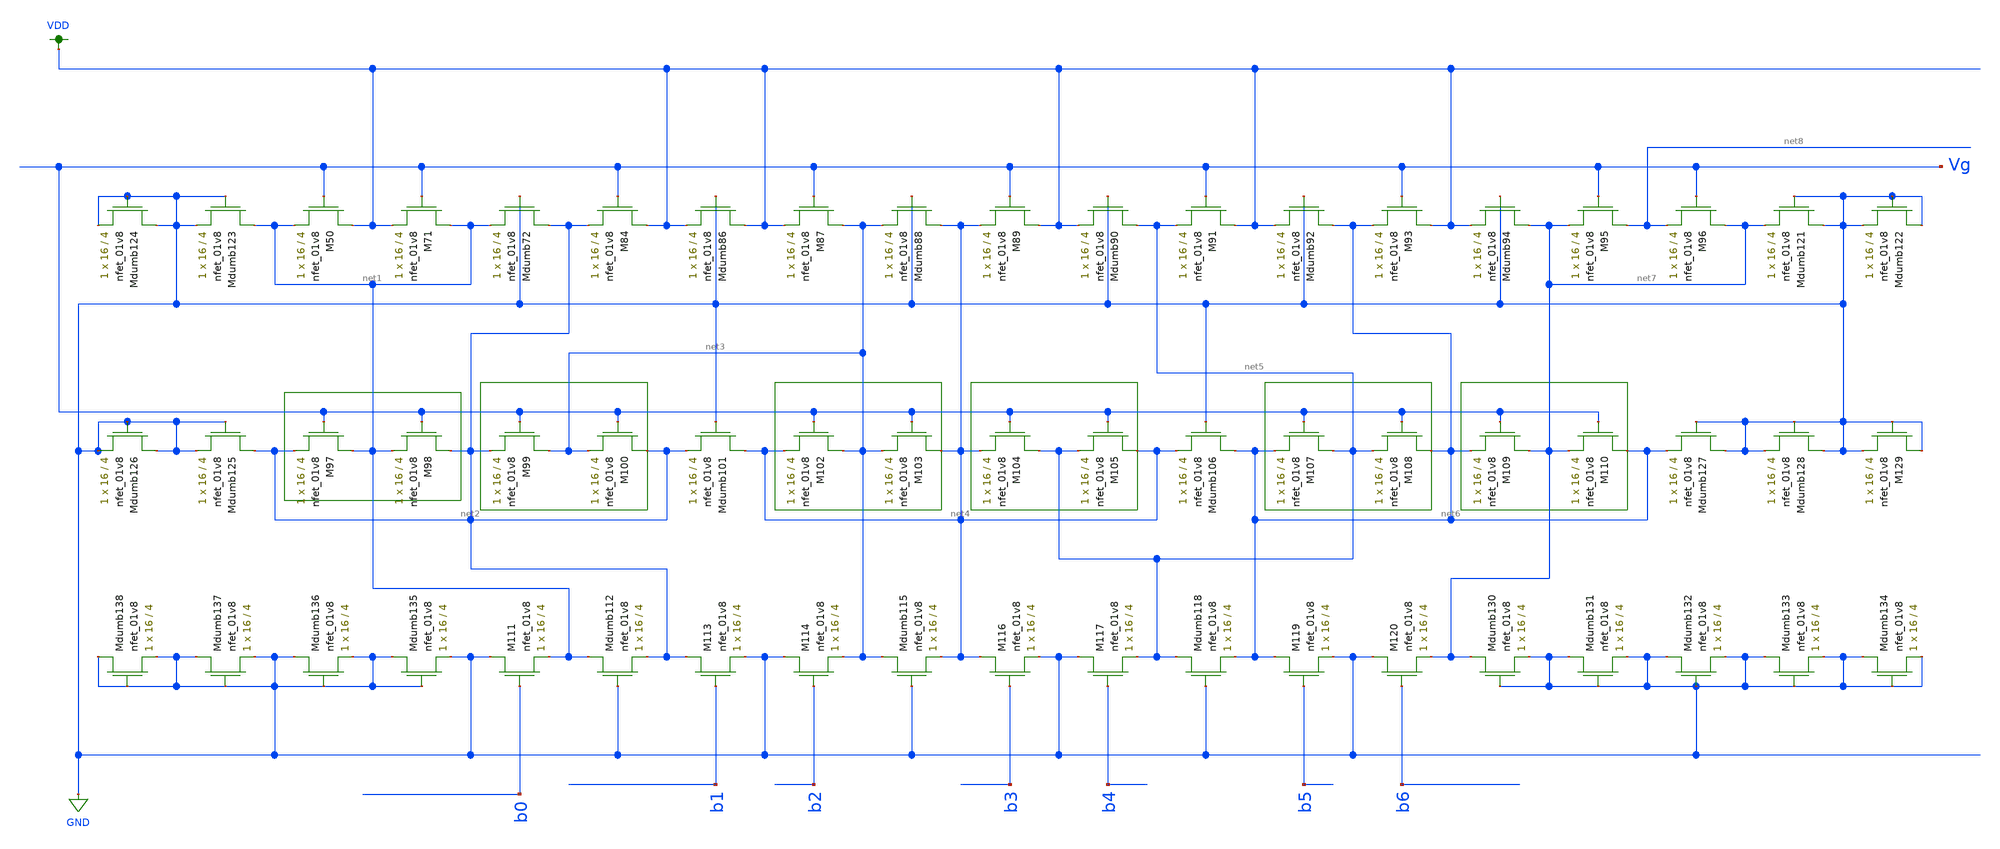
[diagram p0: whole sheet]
** sch_path: schematic/LDS/ladder_lds.sch
**.subckt ladder_lds
XM50 VDD Vg net1 GND sky130_fd_pr__nfet_01v8 L=4 W=16 nf=1 ad='int((nf+1)/2) * W/nf * 0.29' as='int((nf+2)/2) * W/nf * 0.29'
+ pd='2*int((nf+1)/2) * (W/nf + 0.29)' ps='2*int((nf+2)/2) * (W/nf + 0.29)' nrd='0.29 / W' nrs='0.29 / W'
+ sa=0 sb=0 sd=0 mult=1 m=1
XM71 net1 Vg VDD GND sky130_fd_pr__nfet_01v8 L=4 W=16 nf=1 ad='int((nf+1)/2) * W/nf * 0.29' as='int((nf+2)/2) * W/nf * 0.29'
+ pd='2*int((nf+1)/2) * (W/nf + 0.29)' ps='2*int((nf+2)/2) * (W/nf + 0.29)' nrd='0.29 / W' nrs='0.29 / W'
+ sa=0 sb=0 sd=0 mult=1 m=1
XMdumb72 net2 GND net1 GND sky130_fd_pr__nfet_01v8 L=4 W=16 nf=1 ad='int((nf+1)/2) * W/nf * 0.29' as='int((nf+2)/2) * W/nf * 0.29'
+ pd='2*int((nf+1)/2) * (W/nf + 0.29)' ps='2*int((nf+2)/2) * (W/nf + 0.29)' nrd='0.29 / W' nrs='0.29 / W'
+ sa=0 sb=0 sd=0 mult=1 m=1
XM84 VDD Vg net2 GND sky130_fd_pr__nfet_01v8 L=4 W=16 nf=1 ad='int((nf+1)/2) * W/nf * 0.29' as='int((nf+2)/2) * W/nf * 0.29'
+ pd='2*int((nf+1)/2) * (W/nf + 0.29)' ps='2*int((nf+2)/2) * (W/nf + 0.29)' nrd='0.29 / W' nrs='0.29 / W'
+ sa=0 sb=0 sd=0 mult=1 m=1
XMdumb86 VDD GND VDD GND sky130_fd_pr__nfet_01v8 L=4 W=16 nf=1 ad='int((nf+1)/2) * W/nf * 0.29' as='int((nf+2)/2) * W/nf * 0.29'
+ pd='2*int((nf+1)/2) * (W/nf + 0.29)' ps='2*int((nf+2)/2) * (W/nf + 0.29)' nrd='0.29 / W' nrs='0.29 / W'
+ sa=0 sb=0 sd=0 mult=1 m=1
XM87 net3 Vg VDD GND sky130_fd_pr__nfet_01v8 L=4 W=16 nf=1 ad='int((nf+1)/2) * W/nf * 0.29' as='int((nf+2)/2) * W/nf * 0.29'
+ pd='2*int((nf+1)/2) * (W/nf + 0.29)' ps='2*int((nf+2)/2) * (W/nf + 0.29)' nrd='0.29 / W' nrs='0.29 / W'
+ sa=0 sb=0 sd=0 mult=1 m=1
XMdumb88 net4 GND net3 GND sky130_fd_pr__nfet_01v8 L=4 W=16 nf=1 ad='int((nf+1)/2) * W/nf * 0.29' as='int((nf+2)/2) * W/nf * 0.29'
+ pd='2*int((nf+1)/2) * (W/nf + 0.29)' ps='2*int((nf+2)/2) * (W/nf + 0.29)' nrd='0.29 / W' nrs='0.29 / W'
+ sa=0 sb=0 sd=0 mult=1 m=1
XM89 VDD Vg net4 GND sky130_fd_pr__nfet_01v8 L=4 W=16 nf=1 ad='int((nf+1)/2) * W/nf * 0.29' as='int((nf+2)/2) * W/nf * 0.29'
+ pd='2*int((nf+1)/2) * (W/nf + 0.29)' ps='2*int((nf+2)/2) * (W/nf + 0.29)' nrd='0.29 / W' nrs='0.29 / W'
+ sa=0 sb=0 sd=0 mult=1 m=1
XMdumb90 net5 GND VDD GND sky130_fd_pr__nfet_01v8 L=4 W=16 nf=1 ad='int((nf+1)/2) * W/nf * 0.29' as='int((nf+2)/2) * W/nf * 0.29'
+ pd='2*int((nf+1)/2) * (W/nf + 0.29)' ps='2*int((nf+2)/2) * (W/nf + 0.29)' nrd='0.29 / W' nrs='0.29 / W'
+ sa=0 sb=0 sd=0 mult=1 m=1
XM91 VDD Vg net5 GND sky130_fd_pr__nfet_01v8 L=4 W=16 nf=1 ad='int((nf+1)/2) * W/nf * 0.29' as='int((nf+2)/2) * W/nf * 0.29'
+ pd='2*int((nf+1)/2) * (W/nf + 0.29)' ps='2*int((nf+2)/2) * (W/nf + 0.29)' nrd='0.29 / W' nrs='0.29 / W'
+ sa=0 sb=0 sd=0 mult=1 m=1
XMdumb92 net6 GND VDD GND sky130_fd_pr__nfet_01v8 L=4 W=16 nf=1 ad='int((nf+1)/2) * W/nf * 0.29' as='int((nf+2)/2) * W/nf * 0.29'
+ pd='2*int((nf+1)/2) * (W/nf + 0.29)' ps='2*int((nf+2)/2) * (W/nf + 0.29)' nrd='0.29 / W' nrs='0.29 / W'
+ sa=0 sb=0 sd=0 mult=1 m=1
XM93 VDD Vg net6 GND sky130_fd_pr__nfet_01v8 L=4 W=16 nf=1 ad='int((nf+1)/2) * W/nf * 0.29' as='int((nf+2)/2) * W/nf * 0.29'
+ pd='2*int((nf+1)/2) * (W/nf + 0.29)' ps='2*int((nf+2)/2) * (W/nf + 0.29)' nrd='0.29 / W' nrs='0.29 / W'
+ sa=0 sb=0 sd=0 mult=1 m=1
XMdumb94 net7 GND VDD GND sky130_fd_pr__nfet_01v8 L=4 W=16 nf=1 ad='int((nf+1)/2) * W/nf * 0.29' as='int((nf+2)/2) * W/nf * 0.29'
+ pd='2*int((nf+1)/2) * (W/nf + 0.29)' ps='2*int((nf+2)/2) * (W/nf + 0.29)' nrd='0.29 / W' nrs='0.29 / W'
+ sa=0 sb=0 sd=0 mult=1 m=1
XM95 net8 Vg net7 GND sky130_fd_pr__nfet_01v8 L=4 W=16 nf=1 ad='int((nf+1)/2) * W/nf * 0.29' as='int((nf+2)/2) * W/nf * 0.29'
+ pd='2*int((nf+1)/2) * (W/nf + 0.29)' ps='2*int((nf+2)/2) * (W/nf + 0.29)' nrd='0.29 / W' nrs='0.29 / W'
+ sa=0 sb=0 sd=0 mult=1 m=1
XM96 net7 Vg net8 GND sky130_fd_pr__nfet_01v8 L=4 W=16 nf=1 ad='int((nf+1)/2) * W/nf * 0.29' as='int((nf+2)/2) * W/nf * 0.29'
+ pd='2*int((nf+1)/2) * (W/nf + 0.29)' ps='2*int((nf+2)/2) * (W/nf + 0.29)' nrd='0.29 / W' nrs='0.29 / W'
+ sa=0 sb=0 sd=0 mult=1 m=1
XM97 net1 Vg net2 GND sky130_fd_pr__nfet_01v8 L=4 W=16 nf=1 ad='int((nf+1)/2) * W/nf * 0.29' as='int((nf+2)/2) * W/nf * 0.29'
+ pd='2*int((nf+1)/2) * (W/nf + 0.29)' ps='2*int((nf+2)/2) * (W/nf + 0.29)' nrd='0.29 / W' nrs='0.29 / W'
+ sa=0 sb=0 sd=0 mult=1 m=1
XM98 net2 Vg net1 GND sky130_fd_pr__nfet_01v8 L=4 W=16 nf=1 ad='int((nf+1)/2) * W/nf * 0.29' as='int((nf+2)/2) * W/nf * 0.29'
+ pd='2*int((nf+1)/2) * (W/nf + 0.29)' ps='2*int((nf+2)/2) * (W/nf + 0.29)' nrd='0.29 / W' nrs='0.29 / W'
+ sa=0 sb=0 sd=0 mult=1 m=1
XM99 net3 Vg net2 GND sky130_fd_pr__nfet_01v8 L=4 W=16 nf=1 ad='int((nf+1)/2) * W/nf * 0.29' as='int((nf+2)/2) * W/nf * 0.29'
+ pd='2*int((nf+1)/2) * (W/nf + 0.29)' ps='2*int((nf+2)/2) * (W/nf + 0.29)' nrd='0.29 / W' nrs='0.29 / W'
+ sa=0 sb=0 sd=0 mult=1 m=1
XM100 net2 Vg net3 GND sky130_fd_pr__nfet_01v8 L=4 W=16 nf=1 ad='int((nf+1)/2) * W/nf * 0.29' as='int((nf+2)/2) * W/nf * 0.29'
+ pd='2*int((nf+1)/2) * (W/nf + 0.29)' ps='2*int((nf+2)/2) * (W/nf + 0.29)' nrd='0.29 / W' nrs='0.29 / W'
+ sa=0 sb=0 sd=0 mult=1 m=1
XMdumb101 net4 GND net2 GND sky130_fd_pr__nfet_01v8 L=4 W=16 nf=1 ad='int((nf+1)/2) * W/nf * 0.29' as='int((nf+2)/2) * W/nf * 0.29'
+ pd='2*int((nf+1)/2) * (W/nf + 0.29)' ps='2*int((nf+2)/2) * (W/nf + 0.29)' nrd='0.29 / W' nrs='0.29 / W'
+ sa=0 sb=0 sd=0 mult=1 m=1
XM102 net3 Vg net4 GND sky130_fd_pr__nfet_01v8 L=4 W=16 nf=1 ad='int((nf+1)/2) * W/nf * 0.29' as='int((nf+2)/2) * W/nf * 0.29'
+ pd='2*int((nf+1)/2) * (W/nf + 0.29)' ps='2*int((nf+2)/2) * (W/nf + 0.29)' nrd='0.29 / W' nrs='0.29 / W'
+ sa=0 sb=0 sd=0 mult=1 m=1
XM103 net4 Vg net3 GND sky130_fd_pr__nfet_01v8 L=4 W=16 nf=1 ad='int((nf+1)/2) * W/nf * 0.29' as='int((nf+2)/2) * W/nf * 0.29'
+ pd='2*int((nf+1)/2) * (W/nf + 0.29)' ps='2*int((nf+2)/2) * (W/nf + 0.29)' nrd='0.29 / W' nrs='0.29 / W'
+ sa=0 sb=0 sd=0 mult=1 m=1
XM104 net5 Vg net4 GND sky130_fd_pr__nfet_01v8 L=4 W=16 nf=1 ad='int((nf+1)/2) * W/nf * 0.29' as='int((nf+2)/2) * W/nf * 0.29'
+ pd='2*int((nf+1)/2) * (W/nf + 0.29)' ps='2*int((nf+2)/2) * (W/nf + 0.29)' nrd='0.29 / W' nrs='0.29 / W'
+ sa=0 sb=0 sd=0 mult=1 m=1
XM105 net4 Vg net5 GND sky130_fd_pr__nfet_01v8 L=4 W=16 nf=1 ad='int((nf+1)/2) * W/nf * 0.29' as='int((nf+2)/2) * W/nf * 0.29'
+ pd='2*int((nf+1)/2) * (W/nf + 0.29)' ps='2*int((nf+2)/2) * (W/nf + 0.29)' nrd='0.29 / W' nrs='0.29 / W'
+ sa=0 sb=0 sd=0 mult=1 m=1
XMdumb106 net6 GND net4 GND sky130_fd_pr__nfet_01v8 L=4 W=16 nf=1 ad='int((nf+1)/2) * W/nf * 0.29' as='int((nf+2)/2) * W/nf * 0.29'
+ pd='2*int((nf+1)/2) * (W/nf + 0.29)' ps='2*int((nf+2)/2) * (W/nf + 0.29)' nrd='0.29 / W' nrs='0.29 / W'
+ sa=0 sb=0 sd=0 mult=1 m=1
XM107 net5 Vg net6 GND sky130_fd_pr__nfet_01v8 L=4 W=16 nf=1 ad='int((nf+1)/2) * W/nf * 0.29' as='int((nf+2)/2) * W/nf * 0.29'
+ pd='2*int((nf+1)/2) * (W/nf + 0.29)' ps='2*int((nf+2)/2) * (W/nf + 0.29)' nrd='0.29 / W' nrs='0.29 / W'
+ sa=0 sb=0 sd=0 mult=1 m=1
XM108 net6 Vg net5 GND sky130_fd_pr__nfet_01v8 L=4 W=16 nf=1 ad='int((nf+1)/2) * W/nf * 0.29' as='int((nf+2)/2) * W/nf * 0.29'
+ pd='2*int((nf+1)/2) * (W/nf + 0.29)' ps='2*int((nf+2)/2) * (W/nf + 0.29)' nrd='0.29 / W' nrs='0.29 / W'
+ sa=0 sb=0 sd=0 mult=1 m=1
XM109 net7 Vg net6 GND sky130_fd_pr__nfet_01v8 L=4 W=16 nf=1 ad='int((nf+1)/2) * W/nf * 0.29' as='int((nf+2)/2) * W/nf * 0.29'
+ pd='2*int((nf+1)/2) * (W/nf + 0.29)' ps='2*int((nf+2)/2) * (W/nf + 0.29)' nrd='0.29 / W' nrs='0.29 / W'
+ sa=0 sb=0 sd=0 mult=1 m=1
XM110 net6 Vg net7 GND sky130_fd_pr__nfet_01v8 L=4 W=16 nf=1 ad='int((nf+1)/2) * W/nf * 0.29' as='int((nf+2)/2) * W/nf * 0.29'
+ pd='2*int((nf+1)/2) * (W/nf + 0.29)' ps='2*int((nf+2)/2) * (W/nf + 0.29)' nrd='0.29 / W' nrs='0.29 / W'
+ sa=0 sb=0 sd=0 mult=1 m=1
XM111 GND b0 net1 GND sky130_fd_pr__nfet_01v8 L=4 W=16 nf=1 ad='int((nf+1)/2) * W/nf * 0.29' as='int((nf+2)/2) * W/nf * 0.29'
+ pd='2*int((nf+1)/2) * (W/nf + 0.29)' ps='2*int((nf+2)/2) * (W/nf + 0.29)' nrd='0.29 / W' nrs='0.29 / W'
+ sa=0 sb=0 sd=0 mult=1 m=1
XMdumb112 net1 GND net2 GND sky130_fd_pr__nfet_01v8 L=4 W=16 nf=1 ad='int((nf+1)/2) * W/nf * 0.29' as='int((nf+2)/2) * W/nf * 0.29'
+ pd='2*int((nf+1)/2) * (W/nf + 0.29)' ps='2*int((nf+2)/2) * (W/nf + 0.29)' nrd='0.29 / W' nrs='0.29 / W'
+ sa=0 sb=0 sd=0 mult=1 m=1
XM113 net2 b1 GND GND sky130_fd_pr__nfet_01v8 L=4 W=16 nf=1 ad='int((nf+1)/2) * W/nf * 0.29' as='int((nf+2)/2) * W/nf * 0.29'
+ pd='2*int((nf+1)/2) * (W/nf + 0.29)' ps='2*int((nf+2)/2) * (W/nf + 0.29)' nrd='0.29 / W' nrs='0.29 / W'
+ sa=0 sb=0 sd=0 mult=1 m=1
XM114 GND b2 net3 GND sky130_fd_pr__nfet_01v8 L=4 W=16 nf=1 ad='int((nf+1)/2) * W/nf * 0.29' as='int((nf+2)/2) * W/nf * 0.29'
+ pd='2*int((nf+1)/2) * (W/nf + 0.29)' ps='2*int((nf+2)/2) * (W/nf + 0.29)' nrd='0.29 / W' nrs='0.29 / W'
+ sa=0 sb=0 sd=0 mult=1 m=1
XMdumb115 net3 GND net4 GND sky130_fd_pr__nfet_01v8 L=4 W=16 nf=1 ad='int((nf+1)/2) * W/nf * 0.29' as='int((nf+2)/2) * W/nf * 0.29'
+ pd='2*int((nf+1)/2) * (W/nf + 0.29)' ps='2*int((nf+2)/2) * (W/nf + 0.29)' nrd='0.29 / W' nrs='0.29 / W'
+ sa=0 sb=0 sd=0 mult=1 m=1
XM116 net4 b3 GND GND sky130_fd_pr__nfet_01v8 L=4 W=16 nf=1 ad='int((nf+1)/2) * W/nf * 0.29' as='int((nf+2)/2) * W/nf * 0.29'
+ pd='2*int((nf+1)/2) * (W/nf + 0.29)' ps='2*int((nf+2)/2) * (W/nf + 0.29)' nrd='0.29 / W' nrs='0.29 / W'
+ sa=0 sb=0 sd=0 mult=1 m=1
XM117 GND b4 net5 GND sky130_fd_pr__nfet_01v8 L=4 W=16 nf=1 ad='int((nf+1)/2) * W/nf * 0.29' as='int((nf+2)/2) * W/nf * 0.29'
+ pd='2*int((nf+1)/2) * (W/nf + 0.29)' ps='2*int((nf+2)/2) * (W/nf + 0.29)' nrd='0.29 / W' nrs='0.29 / W'
+ sa=0 sb=0 sd=0 mult=1 m=1
XMdumb118 net5 GND net6 GND sky130_fd_pr__nfet_01v8 L=4 W=16 nf=1 ad='int((nf+1)/2) * W/nf * 0.29' as='int((nf+2)/2) * W/nf * 0.29'
+ pd='2*int((nf+1)/2) * (W/nf + 0.29)' ps='2*int((nf+2)/2) * (W/nf + 0.29)' nrd='0.29 / W' nrs='0.29 / W'
+ sa=0 sb=0 sd=0 mult=1 m=1
XM119 net6 b5 GND GND sky130_fd_pr__nfet_01v8 L=4 W=16 nf=1 ad='int((nf+1)/2) * W/nf * 0.29' as='int((nf+2)/2) * W/nf * 0.29'
+ pd='2*int((nf+1)/2) * (W/nf + 0.29)' ps='2*int((nf+2)/2) * (W/nf + 0.29)' nrd='0.29 / W' nrs='0.29 / W'
+ sa=0 sb=0 sd=0 mult=1 m=1
XM120 GND b6 net7 GND sky130_fd_pr__nfet_01v8 L=4 W=16 nf=1 ad='int((nf+1)/2) * W/nf * 0.29' as='int((nf+2)/2) * W/nf * 0.29'
+ pd='2*int((nf+1)/2) * (W/nf + 0.29)' ps='2*int((nf+2)/2) * (W/nf + 0.29)' nrd='0.29 / W' nrs='0.29 / W'
+ sa=0 sb=0 sd=0 mult=1 m=1
XMdumb121 GND GND net7 GND sky130_fd_pr__nfet_01v8 L=4 W=16 nf=1 ad='int((nf+1)/2) * W/nf * 0.29' as='int((nf+2)/2) * W/nf * 0.29'
+ pd='2*int((nf+1)/2) * (W/nf + 0.29)' ps='2*int((nf+2)/2) * (W/nf + 0.29)' nrd='0.29 / W' nrs='0.29 / W'
+ sa=0 sb=0 sd=0 mult=1 m=1
XMdumb122 GND GND GND GND sky130_fd_pr__nfet_01v8 L=4 W=16 nf=1 ad='int((nf+1)/2) * W/nf * 0.29' as='int((nf+2)/2) * W/nf * 0.29'
+ pd='2*int((nf+1)/2) * (W/nf + 0.29)' ps='2*int((nf+2)/2) * (W/nf + 0.29)' nrd='0.29 / W' nrs='0.29 / W'
+ sa=0 sb=0 sd=0 mult=1 m=1
XMdumb123 net1 GND GND GND sky130_fd_pr__nfet_01v8 L=4 W=16 nf=1 ad='int((nf+1)/2) * W/nf * 0.29' as='int((nf+2)/2) * W/nf * 0.29'
+ pd='2*int((nf+1)/2) * (W/nf + 0.29)' ps='2*int((nf+2)/2) * (W/nf + 0.29)' nrd='0.29 / W' nrs='0.29 / W'
+ sa=0 sb=0 sd=0 mult=1 m=1
XMdumb124 GND GND GND GND sky130_fd_pr__nfet_01v8 L=4 W=16 nf=1 ad='int((nf+1)/2) * W/nf * 0.29' as='int((nf+2)/2) * W/nf * 0.29'
+ pd='2*int((nf+1)/2) * (W/nf + 0.29)' ps='2*int((nf+2)/2) * (W/nf + 0.29)' nrd='0.29 / W' nrs='0.29 / W'
+ sa=0 sb=0 sd=0 mult=1 m=1
XMdumb125 net2 GND GND GND sky130_fd_pr__nfet_01v8 L=4 W=16 nf=1 ad='int((nf+1)/2) * W/nf * 0.29' as='int((nf+2)/2) * W/nf * 0.29'
+ pd='2*int((nf+1)/2) * (W/nf + 0.29)' ps='2*int((nf+2)/2) * (W/nf + 0.29)' nrd='0.29 / W' nrs='0.29 / W'
+ sa=0 sb=0 sd=0 mult=1 m=1
XMdumb126 GND GND GND GND sky130_fd_pr__nfet_01v8 L=4 W=16 nf=1 ad='int((nf+1)/2) * W/nf * 0.29' as='int((nf+2)/2) * W/nf * 0.29'
+ pd='2*int((nf+1)/2) * (W/nf + 0.29)' ps='2*int((nf+2)/2) * (W/nf + 0.29)' nrd='0.29 / W' nrs='0.29 / W'
+ sa=0 sb=0 sd=0 mult=1 m=1
XMdumb127 GND GND net6 GND sky130_fd_pr__nfet_01v8 L=4 W=16 nf=1 ad='int((nf+1)/2) * W/nf * 0.29' as='int((nf+2)/2) * W/nf * 0.29'
+ pd='2*int((nf+1)/2) * (W/nf + 0.29)' ps='2*int((nf+2)/2) * (W/nf + 0.29)' nrd='0.29 / W' nrs='0.29 / W'
+ sa=0 sb=0 sd=0 mult=1 m=1
XMdumb128 GND GND GND GND sky130_fd_pr__nfet_01v8 L=4 W=16 nf=1 ad='int((nf+1)/2) * W/nf * 0.29' as='int((nf+2)/2) * W/nf * 0.29'
+ pd='2*int((nf+1)/2) * (W/nf + 0.29)' ps='2*int((nf+2)/2) * (W/nf + 0.29)' nrd='0.29 / W' nrs='0.29 / W'
+ sa=0 sb=0 sd=0 mult=1 m=1
XM129 GND GND GND GND sky130_fd_pr__nfet_01v8 L=4 W=16 nf=1 ad='int((nf+1)/2) * W/nf * 0.29' as='int((nf+2)/2) * W/nf * 0.29'
+ pd='2*int((nf+1)/2) * (W/nf + 0.29)' ps='2*int((nf+2)/2) * (W/nf + 0.29)' nrd='0.29 / W' nrs='0.29 / W'
+ sa=0 sb=0 sd=0 mult=1 m=1
XMdumb130 net7 GND GND GND sky130_fd_pr__nfet_01v8 L=4 W=16 nf=1 ad='int((nf+1)/2) * W/nf * 0.29' as='int((nf+2)/2) * W/nf * 0.29'
+ pd='2*int((nf+1)/2) * (W/nf + 0.29)' ps='2*int((nf+2)/2) * (W/nf + 0.29)' nrd='0.29 / W' nrs='0.29 / W'
+ sa=0 sb=0 sd=0 mult=1 m=1
XMdumb131 GND GND GND GND sky130_fd_pr__nfet_01v8 L=4 W=16 nf=1 ad='int((nf+1)/2) * W/nf * 0.29' as='int((nf+2)/2) * W/nf * 0.29'
+ pd='2*int((nf+1)/2) * (W/nf + 0.29)' ps='2*int((nf+2)/2) * (W/nf + 0.29)' nrd='0.29 / W' nrs='0.29 / W'
+ sa=0 sb=0 sd=0 mult=1 m=1
XMdumb132 GND GND GND GND sky130_fd_pr__nfet_01v8 L=4 W=16 nf=1 ad='int((nf+1)/2) * W/nf * 0.29' as='int((nf+2)/2) * W/nf * 0.29'
+ pd='2*int((nf+1)/2) * (W/nf + 0.29)' ps='2*int((nf+2)/2) * (W/nf + 0.29)' nrd='0.29 / W' nrs='0.29 / W'
+ sa=0 sb=0 sd=0 mult=1 m=1
XMdumb133 GND GND GND GND sky130_fd_pr__nfet_01v8 L=4 W=16 nf=1 ad='int((nf+1)/2) * W/nf * 0.29' as='int((nf+2)/2) * W/nf * 0.29'
+ pd='2*int((nf+1)/2) * (W/nf + 0.29)' ps='2*int((nf+2)/2) * (W/nf + 0.29)' nrd='0.29 / W' nrs='0.29 / W'
+ sa=0 sb=0 sd=0 mult=1 m=1
XMdumb134 GND GND GND GND sky130_fd_pr__nfet_01v8 L=4 W=16 nf=1 ad='int((nf+1)/2) * W/nf * 0.29' as='int((nf+2)/2) * W/nf * 0.29'
+ pd='2*int((nf+1)/2) * (W/nf + 0.29)' ps='2*int((nf+2)/2) * (W/nf + 0.29)' nrd='0.29 / W' nrs='0.29 / W'
+ sa=0 sb=0 sd=0 mult=1 m=1
XMdumb135 GND GND GND GND sky130_fd_pr__nfet_01v8 L=4 W=16 nf=1 ad='int((nf+1)/2) * W/nf * 0.29' as='int((nf+2)/2) * W/nf * 0.29'
+ pd='2*int((nf+1)/2) * (W/nf + 0.29)' ps='2*int((nf+2)/2) * (W/nf + 0.29)' nrd='0.29 / W' nrs='0.29 / W'
+ sa=0 sb=0 sd=0 mult=1 m=1
XMdumb136 GND GND GND GND sky130_fd_pr__nfet_01v8 L=4 W=16 nf=1 ad='int((nf+1)/2) * W/nf * 0.29' as='int((nf+2)/2) * W/nf * 0.29'
+ pd='2*int((nf+1)/2) * (W/nf + 0.29)' ps='2*int((nf+2)/2) * (W/nf + 0.29)' nrd='0.29 / W' nrs='0.29 / W'
+ sa=0 sb=0 sd=0 mult=1 m=1
XMdumb137 GND GND GND GND sky130_fd_pr__nfet_01v8 L=4 W=16 nf=1 ad='int((nf+1)/2) * W/nf * 0.29' as='int((nf+2)/2) * W/nf * 0.29'
+ pd='2*int((nf+1)/2) * (W/nf + 0.29)' ps='2*int((nf+2)/2) * (W/nf + 0.29)' nrd='0.29 / W' nrs='0.29 / W'
+ sa=0 sb=0 sd=0 mult=1 m=1
XMdumb138 GND GND GND GND sky130_fd_pr__nfet_01v8 L=4 W=16 nf=1 ad='int((nf+1)/2) * W/nf * 0.29' as='int((nf+2)/2) * W/nf * 0.29'
+ pd='2*int((nf+1)/2) * (W/nf + 0.29)' ps='2*int((nf+2)/2) * (W/nf + 0.29)' nrd='0.29 / W' nrs='0.29 / W'
+ sa=0 sb=0 sd=0 mult=1 m=1
**.ends
.GLOBAL VDD
.GLOBAL GND
.end
